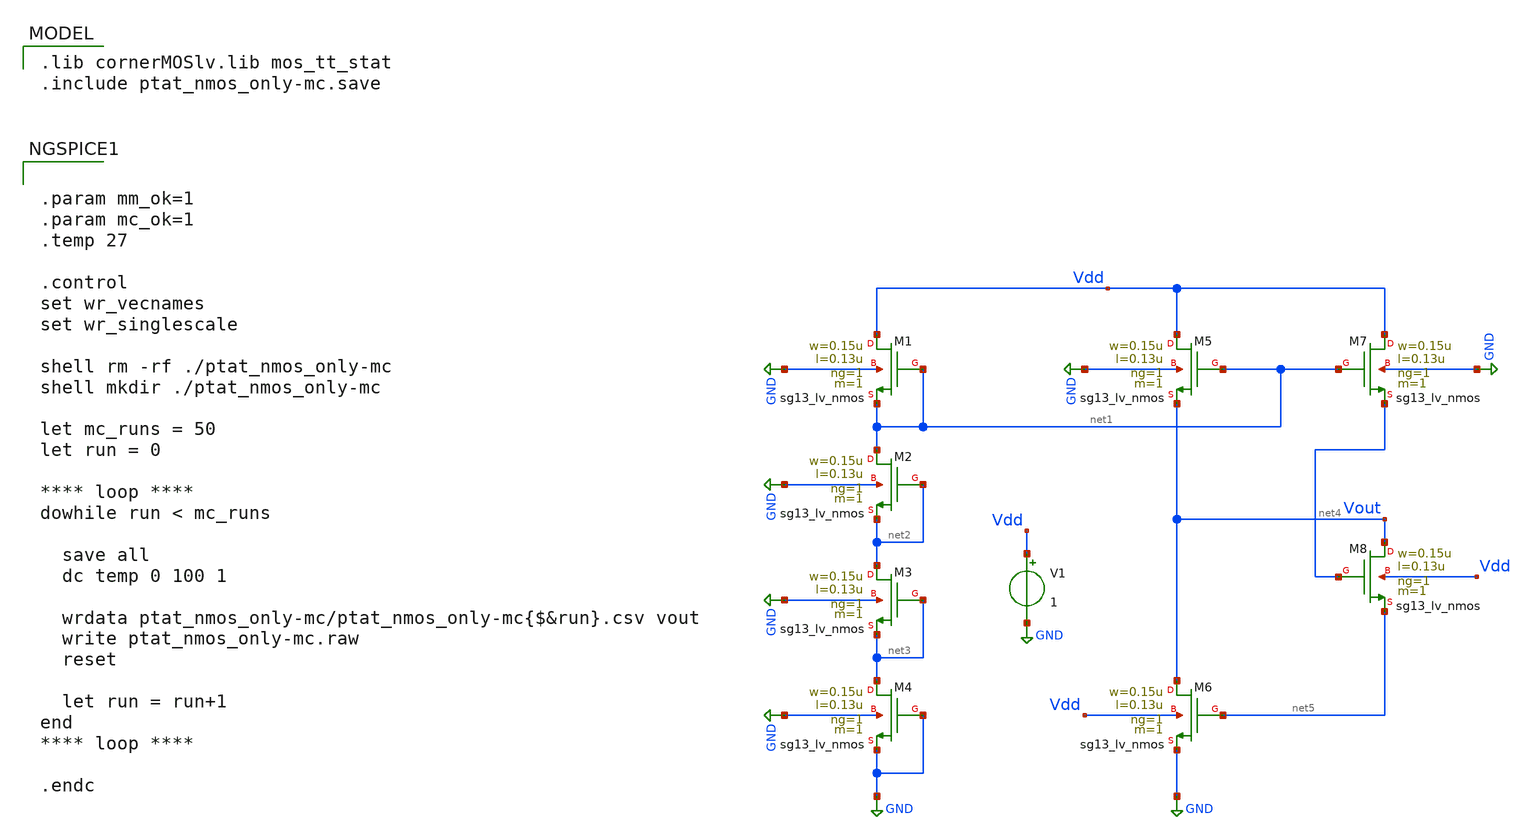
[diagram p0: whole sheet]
** sch_path: TempSensor/design_data/xschem/ptat_nmos_only-mc.sch
**.subckt ptat_nmos_only-mc
XM1 Vdd net1 net1 GND sg13_lv_nmos w=0.15u l=0.13u ng=1 m=1 mm_ok=1
XM2 net1 net2 net2 GND sg13_lv_nmos w=0.15u l=0.13u ng=1 m=1 mm_ok=1
XM3 net2 net3 net3 GND sg13_lv_nmos w=0.15u l=0.13u ng=1 m=1 mm_ok=1
XM4 net3 GND GND GND sg13_lv_nmos w=0.15u l=0.13u ng=1 m=1 mm_ok=1
XM5 Vdd net1 Vout GND sg13_lv_nmos w=0.15u l=0.13u ng=1 m=1 mm_ok=1
XM6 Vout net5 GND Vdd sg13_lv_nmos w=0.15u l=0.13u ng=1 m=1 mm_ok=1
XM7 Vdd net1 net4 GND sg13_lv_nmos w=0.15u l=0.13u ng=1 m=1 mm_ok=1
XM8 Vout net4 net5 Vdd sg13_lv_nmos w=0.15u l=0.13u ng=1 m=1 mm_ok=1
V1 Vdd GND 1
**** begin user architecture code
 .lib cornerMOSlv.lib mos_tt_stat
.include ptat_nmos_only-mc.save



.param mm_ok=1
.param mc_ok=1
.temp 27

.control
set wr_vecnames
set wr_singlescale

shell rm -rf ./ptat_nmos_only-mc
shell mkdir ./ptat_nmos_only-mc

let mc_runs = 50
let run = 0

**** loop ****
dowhile run < mc_runs

  save all
  dc temp 0 100 1

  wrdata ptat_nmos_only-mc/ptat_nmos_only-mc{$&run}.csv vout
  write ptat_nmos_only-mc.raw
  reset

  let run = run+1
end
**** loop ****

.endc


**** end user architecture code
**.ends
.GLOBAL GND
.end
